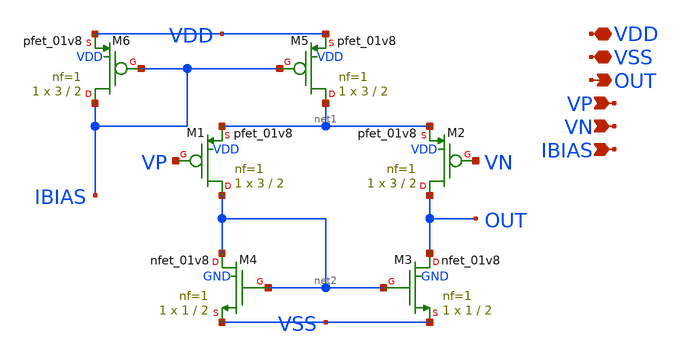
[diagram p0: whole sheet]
** sch_path: designs/libs/core_analog/p-ota/untitled.sch
**.subckt untitled VDD VSS VP VN OUT IBIAS
*.iopin VDD
*.iopin VSS
*.ipin VP
*.ipin VN
*.opin OUT
*.ipin IBIAS
XM1 net2 VP net1 VDD sky130_fd_pr__pfet_01v8 L=2 W=3 nf=1 ad='int((nf+1)/2) * W/nf * 0.29' as='int((nf+2)/2) * W/nf * 0.29'
+ pd='2*int((nf+1)/2) * (W/nf + 0.29)' ps='2*int((nf+2)/2) * (W/nf + 0.29)' nrd='0.29 / W' nrs='0.29 / W'
+ sa=0 sb=0 sd=0 mult=1 m=1
XM2 OUT VN net1 VDD sky130_fd_pr__pfet_01v8 L=2 W=3 nf=1 ad='int((nf+1)/2) * W/nf * 0.29' as='int((nf+2)/2) * W/nf * 0.29'
+ pd='2*int((nf+1)/2) * (W/nf + 0.29)' ps='2*int((nf+2)/2) * (W/nf + 0.29)' nrd='0.29 / W' nrs='0.29 / W'
+ sa=0 sb=0 sd=0 mult=1 m=1
XM3 OUT net2 VSS GND sky130_fd_pr__nfet_01v8 L=2 W=1 nf=1 ad='int((nf+1)/2) * W/nf * 0.29' as='int((nf+2)/2) * W/nf * 0.29'
+ pd='2*int((nf+1)/2) * (W/nf + 0.29)' ps='2*int((nf+2)/2) * (W/nf + 0.29)' nrd='0.29 / W' nrs='0.29 / W'
+ sa=0 sb=0 sd=0 mult=1 m=1
XM4 net2 net2 VSS GND sky130_fd_pr__nfet_01v8 L=2 W=1 nf=1 ad='int((nf+1)/2) * W/nf * 0.29' as='int((nf+2)/2) * W/nf * 0.29'
+ pd='2*int((nf+1)/2) * (W/nf + 0.29)' ps='2*int((nf+2)/2) * (W/nf + 0.29)' nrd='0.29 / W' nrs='0.29 / W'
+ sa=0 sb=0 sd=0 mult=1 m=1
XM5 net1 IBIAS VDD VDD sky130_fd_pr__pfet_01v8 L=2 W=3 nf=1 ad='int((nf+1)/2) * W/nf * 0.29' as='int((nf+2)/2) * W/nf * 0.29'
+ pd='2*int((nf+1)/2) * (W/nf + 0.29)' ps='2*int((nf+2)/2) * (W/nf + 0.29)' nrd='0.29 / W' nrs='0.29 / W'
+ sa=0 sb=0 sd=0 mult=1 m=1
XM6 IBIAS IBIAS VDD VDD sky130_fd_pr__pfet_01v8 L=2 W=3 nf=1 ad='int((nf+1)/2) * W/nf * 0.29' as='int((nf+2)/2) * W/nf * 0.29'
+ pd='2*int((nf+1)/2) * (W/nf + 0.29)' ps='2*int((nf+2)/2) * (W/nf + 0.29)' nrd='0.29 / W' nrs='0.29 / W'
+ sa=0 sb=0 sd=0 mult=1 m=1
**.ends
.end
